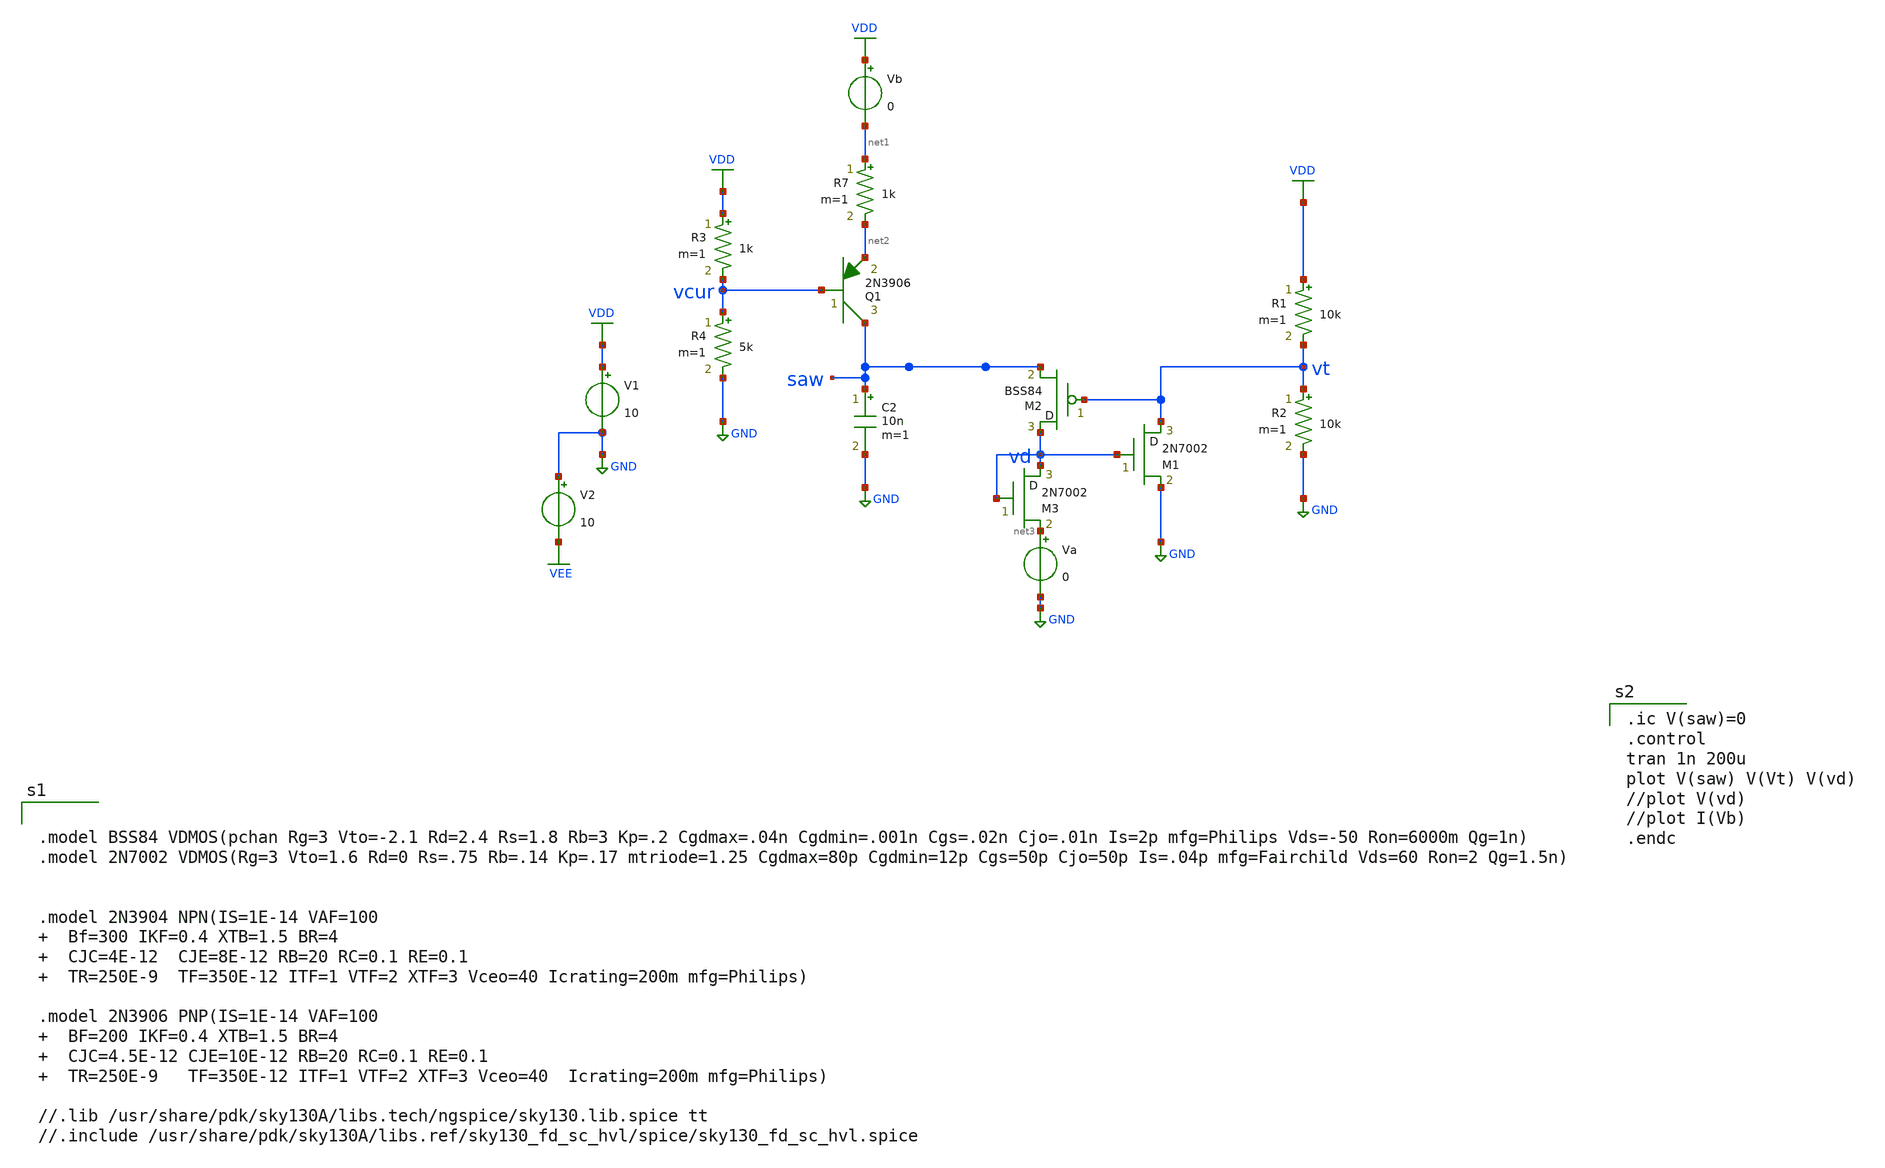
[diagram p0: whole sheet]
** sch_path: xschem/sawgen-fet.sch
**.subckt sawgen-fet
V1 VDD GND 10
M1 vt vd GND 2N7002 m=1
M2 vd vt saw BSS84 m=1
R1 VDD vt 10k m=1
R2 vt GND 10k m=1
C2 saw GND 10n m=1
Q1 saw vcur net2 2N3906 area=1 m=1
R3 VDD vcur 1k m=1
R4 vcur GND 5k m=1
R7 net1 net2 1k m=1
Va net3 GND 0
Vb VDD net1 0
V2 GND VEE 10
M3 vd vd net3 2N7002 m=1
**** begin user architecture code


.model BSS84 VDMOS(pchan Rg=3 Vto=-2.1 Rd=2.4 Rs=1.8 Rb=3 Kp=.2 Cgdmax=.04n Cgdmin=.001n Cgs=.02n
+ Cjo=.01n Is=2p mfg=Philips Vds=-50 Ron=6000m Qg=1n)
.model 2N7002 VDMOS(Rg=3 Vto=1.6 Rd=0 Rs=.75 Rb=.14 Kp=.17 mtriode=1.25 Cgdmax=80p Cgdmin=12p
+ Cgs=50p Cjo=50p Is=.04p mfg=Fairchild Vds=60 Ron=2 Qg=1.5n)


.model 2N3904 NPN(IS=1E-14 VAF=100   Bf=300 IKF=0.4 XTB=1.5 BR=4   CJC=4E-12  CJE=8E-12 RB=20 RC=0.1
+ RE=0.1   TR=250E-9  TF=350E-12 ITF=1 VTF=2 XTF=3 Vceo=40 Icrating=200m mfg=Philips)

.model 2N3906 PNP(IS=1E-14 VAF=100   BF=200 IKF=0.4 XTB=1.5 BR=4   CJC=4.5E-12 CJE=10E-12 RB=20
+ RC=0.1 RE=0.1   TR=250E-9   TF=350E-12 ITF=1 VTF=2 XTF=3 Vceo=40  Icrating=200m mfg=Philips)

//.lib /usr/share/pdk/sky130A/libs.tech/ngspice/sky130.lib.spice tt
//.include /usr/share/pdk/sky130A/libs.ref/sky130_fd_sc_hvl/spice/sky130_fd_sc_hvl.spice


.ic V(saw)=0
.control
tran 1n 200u
plot V(saw) V(Vt) V(vd)
//plot V(vd)
//plot I(Vb)
.endc

**** end user architecture code
**.ends
.GLOBAL VDD
.GLOBAL GND
.GLOBAL VEE
.end
